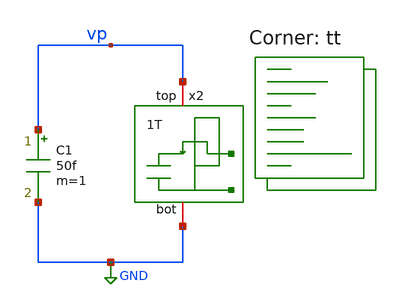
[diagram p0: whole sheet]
** sch_path: xschem/tb/dschr_nwk_type_c_tb.sch
**.subckt dschr_nwk_type_c_tb
C1 vp GND 50f m=1
x2 vp GND dschr_nwk_type_c L=0.15 W=0.5
**** begin user architecture code
.lib $::SKYWATER_MODELS/sky130.lib.spice tt


.include $::netlist_dir/ctrl_sims.spice


**** end user architecture code
**.ends

* expanding   symbol:  dschr_nwks/dschr_nwk_type_c.sym # of pins=2
** sym_path: xschem/dschr_nwks/dschr_nwk_type_c.sym
** sch_path: xschem/dschr_nwks/dschr_nwk_type_c.sch
.subckt dschr_nwk_type_c top bot  L=0.18 W=1
*.iopin top
*.iopin bot
XM1 top bot net1 bot sky130_fd_pr__nfet_01v8 L='L' W='W' nf=1 ad='int((nf+1)/2) * W/nf * 0.29' as='int((nf+2)/2) * W/nf * 0.29'
+ pd='2*int((nf+1)/2) * (W/nf + 0.29)' ps='2*int((nf+2)/2) * (W/nf + 0.29)' nrd='0.29 / W' nrs='0.29 / W'
+ sa=0 sb=0 sd=0 mult=1 m=1
C2 net1 bot 1p m=1
.ends

.GLOBAL GND
.end
